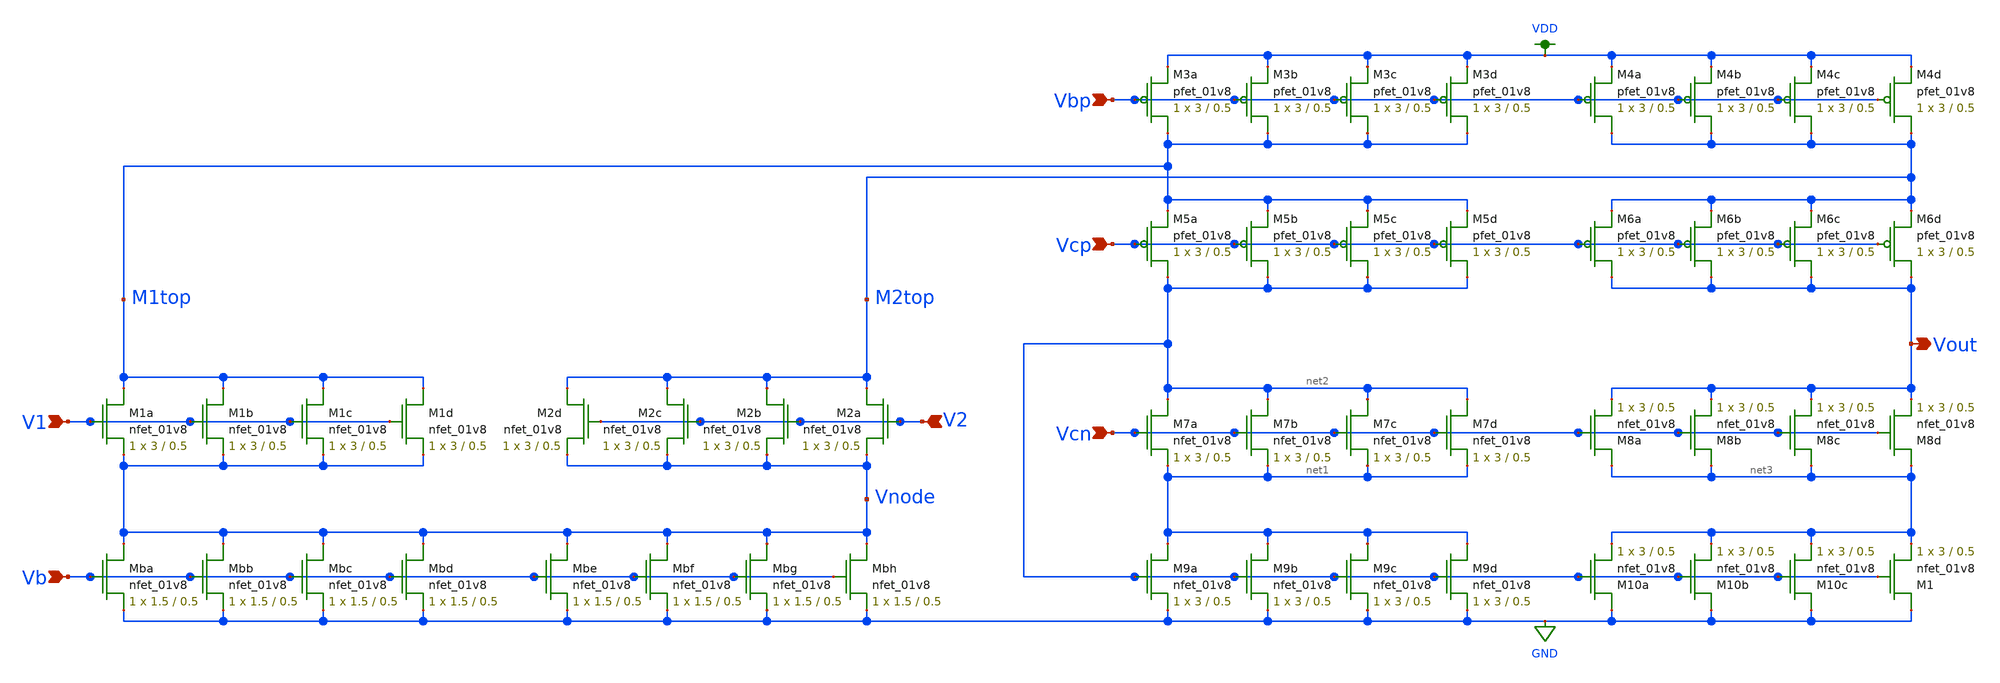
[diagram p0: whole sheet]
** sch_path: mp3/xschem/opamp_schematic_lvs.sch
**.subckt opamp_schematic_lvs Vbp Vcp Vcn V2 V1 Vb Vout
*.ipin Vbp
*.ipin Vcp
*.ipin Vcn
*.ipin V2
*.ipin V1
*.ipin Vb
*.opin Vout
XM1a M1top V1 Vnode GND sky130_fd_pr__nfet_01v8 L=0.5 W=3 nf=1 ad='int((nf+1)/2) * W/nf * 0.29' as='int((nf+2)/2) * W/nf * 0.29'
+ pd='2*int((nf+1)/2) * (W/nf + 0.29)' ps='2*int((nf+2)/2) * (W/nf + 0.29)' nrd='0.29 / W' nrs='0.29 / W'
+ sa=0 sb=0 sd=0 mult=1 m=1
XM1b M1top V1 Vnode GND sky130_fd_pr__nfet_01v8 L=0.5 W=3 nf=1 ad='int((nf+1)/2) * W/nf * 0.29' as='int((nf+2)/2) * W/nf * 0.29'
+ pd='2*int((nf+1)/2) * (W/nf + 0.29)' ps='2*int((nf+2)/2) * (W/nf + 0.29)' nrd='0.29 / W' nrs='0.29 / W'
+ sa=0 sb=0 sd=0 mult=1 m=1
XM1c M1top V1 Vnode GND sky130_fd_pr__nfet_01v8 L=0.5 W=3 nf=1 ad='int((nf+1)/2) * W/nf * 0.29' as='int((nf+2)/2) * W/nf * 0.29'
+ pd='2*int((nf+1)/2) * (W/nf + 0.29)' ps='2*int((nf+2)/2) * (W/nf + 0.29)' nrd='0.29 / W' nrs='0.29 / W'
+ sa=0 sb=0 sd=0 mult=1 m=1
XM1d M1top V1 Vnode GND sky130_fd_pr__nfet_01v8 L=0.5 W=3 nf=1 ad='int((nf+1)/2) * W/nf * 0.29' as='int((nf+2)/2) * W/nf * 0.29'
+ pd='2*int((nf+1)/2) * (W/nf + 0.29)' ps='2*int((nf+2)/2) * (W/nf + 0.29)' nrd='0.29 / W' nrs='0.29 / W'
+ sa=0 sb=0 sd=0 mult=1 m=1
XM2a M2top V2 Vnode GND sky130_fd_pr__nfet_01v8 L=0.5 W=3 nf=1 ad='int((nf+1)/2) * W/nf * 0.29' as='int((nf+2)/2) * W/nf * 0.29'
+ pd='2*int((nf+1)/2) * (W/nf + 0.29)' ps='2*int((nf+2)/2) * (W/nf + 0.29)' nrd='0.29 / W' nrs='0.29 / W'
+ sa=0 sb=0 sd=0 mult=1 m=1
XM2b M2top V2 Vnode GND sky130_fd_pr__nfet_01v8 L=0.5 W=3 nf=1 ad='int((nf+1)/2) * W/nf * 0.29' as='int((nf+2)/2) * W/nf * 0.29'
+ pd='2*int((nf+1)/2) * (W/nf + 0.29)' ps='2*int((nf+2)/2) * (W/nf + 0.29)' nrd='0.29 / W' nrs='0.29 / W'
+ sa=0 sb=0 sd=0 mult=1 m=1
XM2c M2top V2 Vnode GND sky130_fd_pr__nfet_01v8 L=0.5 W=3 nf=1 ad='int((nf+1)/2) * W/nf * 0.29' as='int((nf+2)/2) * W/nf * 0.29'
+ pd='2*int((nf+1)/2) * (W/nf + 0.29)' ps='2*int((nf+2)/2) * (W/nf + 0.29)' nrd='0.29 / W' nrs='0.29 / W'
+ sa=0 sb=0 sd=0 mult=1 m=1
XM2d M2top V2 Vnode GND sky130_fd_pr__nfet_01v8 L=0.5 W=3 nf=1 ad='int((nf+1)/2) * W/nf * 0.29' as='int((nf+2)/2) * W/nf * 0.29'
+ pd='2*int((nf+1)/2) * (W/nf + 0.29)' ps='2*int((nf+2)/2) * (W/nf + 0.29)' nrd='0.29 / W' nrs='0.29 / W'
+ sa=0 sb=0 sd=0 mult=1 m=1
XMba Vnode Vb GND GND sky130_fd_pr__nfet_01v8 L=0.5 W=1.5 nf=1 ad='int((nf+1)/2) * W/nf * 0.29' as='int((nf+2)/2) * W/nf * 0.29'
+ pd='2*int((nf+1)/2) * (W/nf + 0.29)' ps='2*int((nf+2)/2) * (W/nf + 0.29)' nrd='0.29 / W' nrs='0.29 / W'
+ sa=0 sb=0 sd=0 mult=1 m=1
XMbb Vnode Vb GND GND sky130_fd_pr__nfet_01v8 L=0.5 W=1.5 nf=1 ad='int((nf+1)/2) * W/nf * 0.29' as='int((nf+2)/2) * W/nf * 0.29'
+ pd='2*int((nf+1)/2) * (W/nf + 0.29)' ps='2*int((nf+2)/2) * (W/nf + 0.29)' nrd='0.29 / W' nrs='0.29 / W'
+ sa=0 sb=0 sd=0 mult=1 m=1
XMbc Vnode Vb GND GND sky130_fd_pr__nfet_01v8 L=0.5 W=1.5 nf=1 ad='int((nf+1)/2) * W/nf * 0.29' as='int((nf+2)/2) * W/nf * 0.29'
+ pd='2*int((nf+1)/2) * (W/nf + 0.29)' ps='2*int((nf+2)/2) * (W/nf + 0.29)' nrd='0.29 / W' nrs='0.29 / W'
+ sa=0 sb=0 sd=0 mult=1 m=1
XMbd Vnode Vb GND GND sky130_fd_pr__nfet_01v8 L=0.5 W=1.5 nf=1 ad='int((nf+1)/2) * W/nf * 0.29' as='int((nf+2)/2) * W/nf * 0.29'
+ pd='2*int((nf+1)/2) * (W/nf + 0.29)' ps='2*int((nf+2)/2) * (W/nf + 0.29)' nrd='0.29 / W' nrs='0.29 / W'
+ sa=0 sb=0 sd=0 mult=1 m=1
XMbe Vnode Vb GND GND sky130_fd_pr__nfet_01v8 L=0.5 W=1.5 nf=1 ad='int((nf+1)/2) * W/nf * 0.29' as='int((nf+2)/2) * W/nf * 0.29'
+ pd='2*int((nf+1)/2) * (W/nf + 0.29)' ps='2*int((nf+2)/2) * (W/nf + 0.29)' nrd='0.29 / W' nrs='0.29 / W'
+ sa=0 sb=0 sd=0 mult=1 m=1
XMbf Vnode Vb GND GND sky130_fd_pr__nfet_01v8 L=0.5 W=1.5 nf=1 ad='int((nf+1)/2) * W/nf * 0.29' as='int((nf+2)/2) * W/nf * 0.29'
+ pd='2*int((nf+1)/2) * (W/nf + 0.29)' ps='2*int((nf+2)/2) * (W/nf + 0.29)' nrd='0.29 / W' nrs='0.29 / W'
+ sa=0 sb=0 sd=0 mult=1 m=1
XMbg Vnode Vb GND GND sky130_fd_pr__nfet_01v8 L=0.5 W=1.5 nf=1 ad='int((nf+1)/2) * W/nf * 0.29' as='int((nf+2)/2) * W/nf * 0.29'
+ pd='2*int((nf+1)/2) * (W/nf + 0.29)' ps='2*int((nf+2)/2) * (W/nf + 0.29)' nrd='0.29 / W' nrs='0.29 / W'
+ sa=0 sb=0 sd=0 mult=1 m=1
XMbh Vnode Vb GND GND sky130_fd_pr__nfet_01v8 L=0.5 W=1.5 nf=1 ad='int((nf+1)/2) * W/nf * 0.29' as='int((nf+2)/2) * W/nf * 0.29'
+ pd='2*int((nf+1)/2) * (W/nf + 0.29)' ps='2*int((nf+2)/2) * (W/nf + 0.29)' nrd='0.29 / W' nrs='0.29 / W'
+ sa=0 sb=0 sd=0 mult=1 m=1
XM7a net2 Vcn net1 GND sky130_fd_pr__nfet_01v8 L=0.5 W=3 nf=1 ad='int((nf+1)/2) * W/nf * 0.29' as='int((nf+2)/2) * W/nf * 0.29'
+ pd='2*int((nf+1)/2) * (W/nf + 0.29)' ps='2*int((nf+2)/2) * (W/nf + 0.29)' nrd='0.29 / W' nrs='0.29 / W'
+ sa=0 sb=0 sd=0 mult=1 m=1
XM7b net2 Vcn net1 GND sky130_fd_pr__nfet_01v8 L=0.5 W=3 nf=1 ad='int((nf+1)/2) * W/nf * 0.29' as='int((nf+2)/2) * W/nf * 0.29'
+ pd='2*int((nf+1)/2) * (W/nf + 0.29)' ps='2*int((nf+2)/2) * (W/nf + 0.29)' nrd='0.29 / W' nrs='0.29 / W'
+ sa=0 sb=0 sd=0 mult=1 m=1
XM7c net2 Vcn net1 GND sky130_fd_pr__nfet_01v8 L=0.5 W=3 nf=1 ad='int((nf+1)/2) * W/nf * 0.29' as='int((nf+2)/2) * W/nf * 0.29'
+ pd='2*int((nf+1)/2) * (W/nf + 0.29)' ps='2*int((nf+2)/2) * (W/nf + 0.29)' nrd='0.29 / W' nrs='0.29 / W'
+ sa=0 sb=0 sd=0 mult=1 m=1
XM7d net2 Vcn net1 GND sky130_fd_pr__nfet_01v8 L=0.5 W=3 nf=1 ad='int((nf+1)/2) * W/nf * 0.29' as='int((nf+2)/2) * W/nf * 0.29'
+ pd='2*int((nf+1)/2) * (W/nf + 0.29)' ps='2*int((nf+2)/2) * (W/nf + 0.29)' nrd='0.29 / W' nrs='0.29 / W'
+ sa=0 sb=0 sd=0 mult=1 m=1
XM8a net3 Vcn Vout GND sky130_fd_pr__nfet_01v8 L=0.5 W=3 nf=1 ad='int((nf+1)/2) * W/nf * 0.29' as='int((nf+2)/2) * W/nf * 0.29'
+ pd='2*int((nf+1)/2) * (W/nf + 0.29)' ps='2*int((nf+2)/2) * (W/nf + 0.29)' nrd='0.29 / W' nrs='0.29 / W'
+ sa=0 sb=0 sd=0 mult=1 m=1
XM8b net3 Vcn Vout GND sky130_fd_pr__nfet_01v8 L=0.5 W=3 nf=1 ad='int((nf+1)/2) * W/nf * 0.29' as='int((nf+2)/2) * W/nf * 0.29'
+ pd='2*int((nf+1)/2) * (W/nf + 0.29)' ps='2*int((nf+2)/2) * (W/nf + 0.29)' nrd='0.29 / W' nrs='0.29 / W'
+ sa=0 sb=0 sd=0 mult=1 m=1
XM8c net3 Vcn Vout GND sky130_fd_pr__nfet_01v8 L=0.5 W=3 nf=1 ad='int((nf+1)/2) * W/nf * 0.29' as='int((nf+2)/2) * W/nf * 0.29'
+ pd='2*int((nf+1)/2) * (W/nf + 0.29)' ps='2*int((nf+2)/2) * (W/nf + 0.29)' nrd='0.29 / W' nrs='0.29 / W'
+ sa=0 sb=0 sd=0 mult=1 m=1
XM8d net3 Vcn Vout GND sky130_fd_pr__nfet_01v8 L=0.5 W=3 nf=1 ad='int((nf+1)/2) * W/nf * 0.29' as='int((nf+2)/2) * W/nf * 0.29'
+ pd='2*int((nf+1)/2) * (W/nf + 0.29)' ps='2*int((nf+2)/2) * (W/nf + 0.29)' nrd='0.29 / W' nrs='0.29 / W'
+ sa=0 sb=0 sd=0 mult=1 m=1
XM9a net1 net2 GND GND sky130_fd_pr__nfet_01v8 L=0.5 W=3 nf=1 ad='int((nf+1)/2) * W/nf * 0.29' as='int((nf+2)/2) * W/nf * 0.29'
+ pd='2*int((nf+1)/2) * (W/nf + 0.29)' ps='2*int((nf+2)/2) * (W/nf + 0.29)' nrd='0.29 / W' nrs='0.29 / W'
+ sa=0 sb=0 sd=0 mult=1 m=1
XM9b net1 net2 GND GND sky130_fd_pr__nfet_01v8 L=0.5 W=3 nf=1 ad='int((nf+1)/2) * W/nf * 0.29' as='int((nf+2)/2) * W/nf * 0.29'
+ pd='2*int((nf+1)/2) * (W/nf + 0.29)' ps='2*int((nf+2)/2) * (W/nf + 0.29)' nrd='0.29 / W' nrs='0.29 / W'
+ sa=0 sb=0 sd=0 mult=1 m=1
XM9c net1 net2 GND GND sky130_fd_pr__nfet_01v8 L=0.5 W=3 nf=1 ad='int((nf+1)/2) * W/nf * 0.29' as='int((nf+2)/2) * W/nf * 0.29'
+ pd='2*int((nf+1)/2) * (W/nf + 0.29)' ps='2*int((nf+2)/2) * (W/nf + 0.29)' nrd='0.29 / W' nrs='0.29 / W'
+ sa=0 sb=0 sd=0 mult=1 m=1
XM9d net1 net2 GND GND sky130_fd_pr__nfet_01v8 L=0.5 W=3 nf=1 ad='int((nf+1)/2) * W/nf * 0.29' as='int((nf+2)/2) * W/nf * 0.29'
+ pd='2*int((nf+1)/2) * (W/nf + 0.29)' ps='2*int((nf+2)/2) * (W/nf + 0.29)' nrd='0.29 / W' nrs='0.29 / W'
+ sa=0 sb=0 sd=0 mult=1 m=1
XM10a GND net2 net3 GND sky130_fd_pr__nfet_01v8 L=0.5 W=3 nf=1 ad='int((nf+1)/2) * W/nf * 0.29' as='int((nf+2)/2) * W/nf * 0.29'
+ pd='2*int((nf+1)/2) * (W/nf + 0.29)' ps='2*int((nf+2)/2) * (W/nf + 0.29)' nrd='0.29 / W' nrs='0.29 / W'
+ sa=0 sb=0 sd=0 mult=1 m=1
XM10b GND net2 net3 GND sky130_fd_pr__nfet_01v8 L=0.5 W=3 nf=1 ad='int((nf+1)/2) * W/nf * 0.29' as='int((nf+2)/2) * W/nf * 0.29'
+ pd='2*int((nf+1)/2) * (W/nf + 0.29)' ps='2*int((nf+2)/2) * (W/nf + 0.29)' nrd='0.29 / W' nrs='0.29 / W'
+ sa=0 sb=0 sd=0 mult=1 m=1
XM10c GND net2 net3 GND sky130_fd_pr__nfet_01v8 L=0.5 W=3 nf=1 ad='int((nf+1)/2) * W/nf * 0.29' as='int((nf+2)/2) * W/nf * 0.29'
+ pd='2*int((nf+1)/2) * (W/nf + 0.29)' ps='2*int((nf+2)/2) * (W/nf + 0.29)' nrd='0.29 / W' nrs='0.29 / W'
+ sa=0 sb=0 sd=0 mult=1 m=1
XM1 GND net2 net3 GND sky130_fd_pr__nfet_01v8 L=0.5 W=3 nf=1 ad='int((nf+1)/2) * W/nf * 0.29' as='int((nf+2)/2) * W/nf * 0.29'
+ pd='2*int((nf+1)/2) * (W/nf + 0.29)' ps='2*int((nf+2)/2) * (W/nf + 0.29)' nrd='0.29 / W' nrs='0.29 / W'
+ sa=0 sb=0 sd=0 mult=1 m=1
XM5a net2 Vcp M1top VDD sky130_fd_pr__pfet_01v8 L=0.5 W=3 nf=1 ad='int((nf+1)/2) * W/nf * 0.29' as='int((nf+2)/2) * W/nf * 0.29'
+ pd='2*int((nf+1)/2) * (W/nf + 0.29)' ps='2*int((nf+2)/2) * (W/nf + 0.29)' nrd='0.29 / W' nrs='0.29 / W'
+ sa=0 sb=0 sd=0 mult=1 m=1
XM5b net2 Vcp M1top VDD sky130_fd_pr__pfet_01v8 L=0.5 W=3 nf=1 ad='int((nf+1)/2) * W/nf * 0.29' as='int((nf+2)/2) * W/nf * 0.29'
+ pd='2*int((nf+1)/2) * (W/nf + 0.29)' ps='2*int((nf+2)/2) * (W/nf + 0.29)' nrd='0.29 / W' nrs='0.29 / W'
+ sa=0 sb=0 sd=0 mult=1 m=1
XM5c net2 Vcp M1top VDD sky130_fd_pr__pfet_01v8 L=0.5 W=3 nf=1 ad='int((nf+1)/2) * W/nf * 0.29' as='int((nf+2)/2) * W/nf * 0.29'
+ pd='2*int((nf+1)/2) * (W/nf + 0.29)' ps='2*int((nf+2)/2) * (W/nf + 0.29)' nrd='0.29 / W' nrs='0.29 / W'
+ sa=0 sb=0 sd=0 mult=1 m=1
XM5d net2 Vcp M1top VDD sky130_fd_pr__pfet_01v8 L=0.5 W=3 nf=1 ad='int((nf+1)/2) * W/nf * 0.29' as='int((nf+2)/2) * W/nf * 0.29'
+ pd='2*int((nf+1)/2) * (W/nf + 0.29)' ps='2*int((nf+2)/2) * (W/nf + 0.29)' nrd='0.29 / W' nrs='0.29 / W'
+ sa=0 sb=0 sd=0 mult=1 m=1
XM6a Vout Vcp M2top VDD sky130_fd_pr__pfet_01v8 L=0.5 W=3 nf=1 ad='int((nf+1)/2) * W/nf * 0.29' as='int((nf+2)/2) * W/nf * 0.29'
+ pd='2*int((nf+1)/2) * (W/nf + 0.29)' ps='2*int((nf+2)/2) * (W/nf + 0.29)' nrd='0.29 / W' nrs='0.29 / W'
+ sa=0 sb=0 sd=0 mult=1 m=1
XM6b Vout Vcp M2top VDD sky130_fd_pr__pfet_01v8 L=0.5 W=3 nf=1 ad='int((nf+1)/2) * W/nf * 0.29' as='int((nf+2)/2) * W/nf * 0.29'
+ pd='2*int((nf+1)/2) * (W/nf + 0.29)' ps='2*int((nf+2)/2) * (W/nf + 0.29)' nrd='0.29 / W' nrs='0.29 / W'
+ sa=0 sb=0 sd=0 mult=1 m=1
XM6c Vout Vcp M2top VDD sky130_fd_pr__pfet_01v8 L=0.5 W=3 nf=1 ad='int((nf+1)/2) * W/nf * 0.29' as='int((nf+2)/2) * W/nf * 0.29'
+ pd='2*int((nf+1)/2) * (W/nf + 0.29)' ps='2*int((nf+2)/2) * (W/nf + 0.29)' nrd='0.29 / W' nrs='0.29 / W'
+ sa=0 sb=0 sd=0 mult=1 m=1
XM6d Vout Vcp M2top VDD sky130_fd_pr__pfet_01v8 L=0.5 W=3 nf=1 ad='int((nf+1)/2) * W/nf * 0.29' as='int((nf+2)/2) * W/nf * 0.29'
+ pd='2*int((nf+1)/2) * (W/nf + 0.29)' ps='2*int((nf+2)/2) * (W/nf + 0.29)' nrd='0.29 / W' nrs='0.29 / W'
+ sa=0 sb=0 sd=0 mult=1 m=1
XM3a M1top Vbp VDD VDD sky130_fd_pr__pfet_01v8 L=0.5 W=3 nf=1 ad='int((nf+1)/2) * W/nf * 0.29' as='int((nf+2)/2) * W/nf * 0.29'
+ pd='2*int((nf+1)/2) * (W/nf + 0.29)' ps='2*int((nf+2)/2) * (W/nf + 0.29)' nrd='0.29 / W' nrs='0.29 / W'
+ sa=0 sb=0 sd=0 mult=1 m=1
XM3b M1top Vbp VDD VDD sky130_fd_pr__pfet_01v8 L=0.5 W=3 nf=1 ad='int((nf+1)/2) * W/nf * 0.29' as='int((nf+2)/2) * W/nf * 0.29'
+ pd='2*int((nf+1)/2) * (W/nf + 0.29)' ps='2*int((nf+2)/2) * (W/nf + 0.29)' nrd='0.29 / W' nrs='0.29 / W'
+ sa=0 sb=0 sd=0 mult=1 m=1
XM3c M1top Vbp VDD VDD sky130_fd_pr__pfet_01v8 L=0.5 W=3 nf=1 ad='int((nf+1)/2) * W/nf * 0.29' as='int((nf+2)/2) * W/nf * 0.29'
+ pd='2*int((nf+1)/2) * (W/nf + 0.29)' ps='2*int((nf+2)/2) * (W/nf + 0.29)' nrd='0.29 / W' nrs='0.29 / W'
+ sa=0 sb=0 sd=0 mult=1 m=1
XM3d M1top Vbp VDD VDD sky130_fd_pr__pfet_01v8 L=0.5 W=3 nf=1 ad='int((nf+1)/2) * W/nf * 0.29' as='int((nf+2)/2) * W/nf * 0.29'
+ pd='2*int((nf+1)/2) * (W/nf + 0.29)' ps='2*int((nf+2)/2) * (W/nf + 0.29)' nrd='0.29 / W' nrs='0.29 / W'
+ sa=0 sb=0 sd=0 mult=1 m=1
XM4a M2top Vbp VDD VDD sky130_fd_pr__pfet_01v8 L=0.5 W=3 nf=1 ad='int((nf+1)/2) * W/nf * 0.29' as='int((nf+2)/2) * W/nf * 0.29'
+ pd='2*int((nf+1)/2) * (W/nf + 0.29)' ps='2*int((nf+2)/2) * (W/nf + 0.29)' nrd='0.29 / W' nrs='0.29 / W'
+ sa=0 sb=0 sd=0 mult=1 m=1
XM4b M2top Vbp VDD VDD sky130_fd_pr__pfet_01v8 L=0.5 W=3 nf=1 ad='int((nf+1)/2) * W/nf * 0.29' as='int((nf+2)/2) * W/nf * 0.29'
+ pd='2*int((nf+1)/2) * (W/nf + 0.29)' ps='2*int((nf+2)/2) * (W/nf + 0.29)' nrd='0.29 / W' nrs='0.29 / W'
+ sa=0 sb=0 sd=0 mult=1 m=1
XM4c M2top Vbp VDD VDD sky130_fd_pr__pfet_01v8 L=0.5 W=3 nf=1 ad='int((nf+1)/2) * W/nf * 0.29' as='int((nf+2)/2) * W/nf * 0.29'
+ pd='2*int((nf+1)/2) * (W/nf + 0.29)' ps='2*int((nf+2)/2) * (W/nf + 0.29)' nrd='0.29 / W' nrs='0.29 / W'
+ sa=0 sb=0 sd=0 mult=1 m=1
XM4d M2top Vbp VDD VDD sky130_fd_pr__pfet_01v8 L=0.5 W=3 nf=1 ad='int((nf+1)/2) * W/nf * 0.29' as='int((nf+2)/2) * W/nf * 0.29'
+ pd='2*int((nf+1)/2) * (W/nf + 0.29)' ps='2*int((nf+2)/2) * (W/nf + 0.29)' nrd='0.29 / W' nrs='0.29 / W'
+ sa=0 sb=0 sd=0 mult=1 m=1
**.ends
.GLOBAL VDD
.GLOBAL GND
.end
